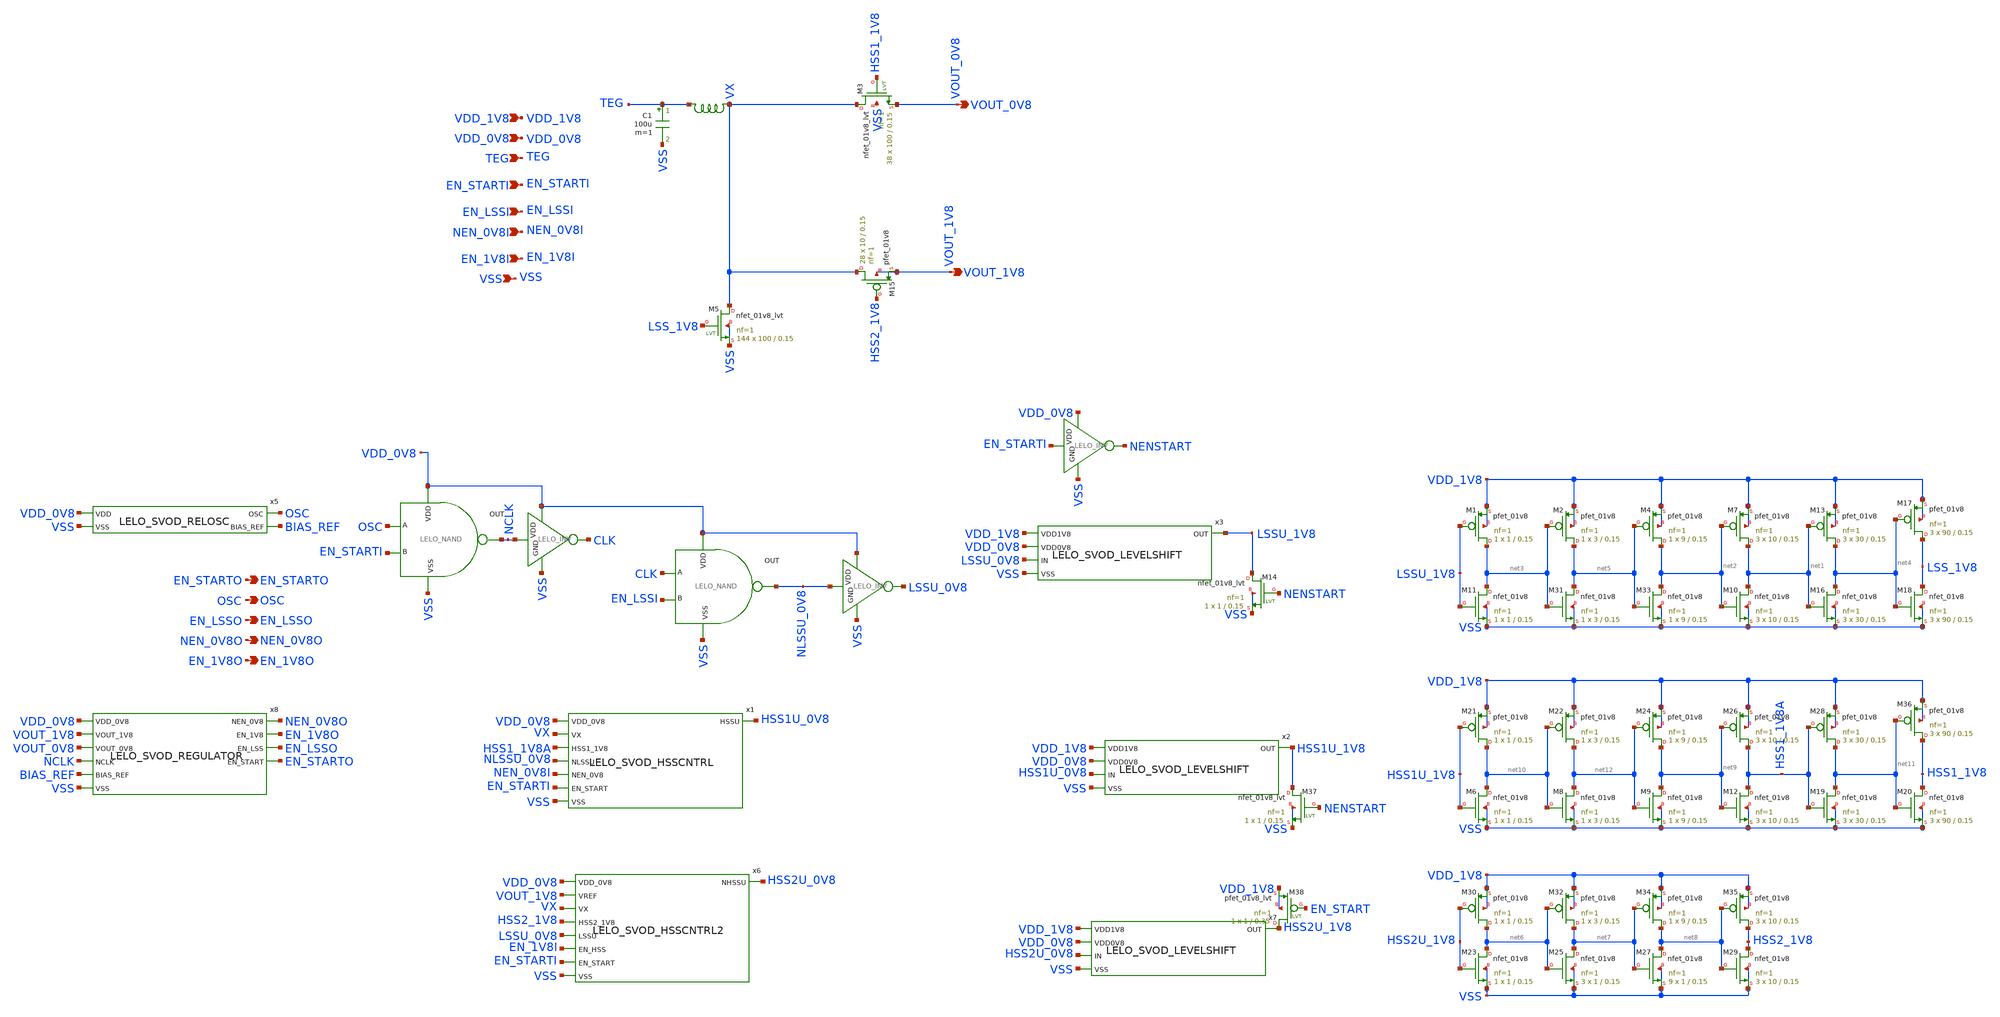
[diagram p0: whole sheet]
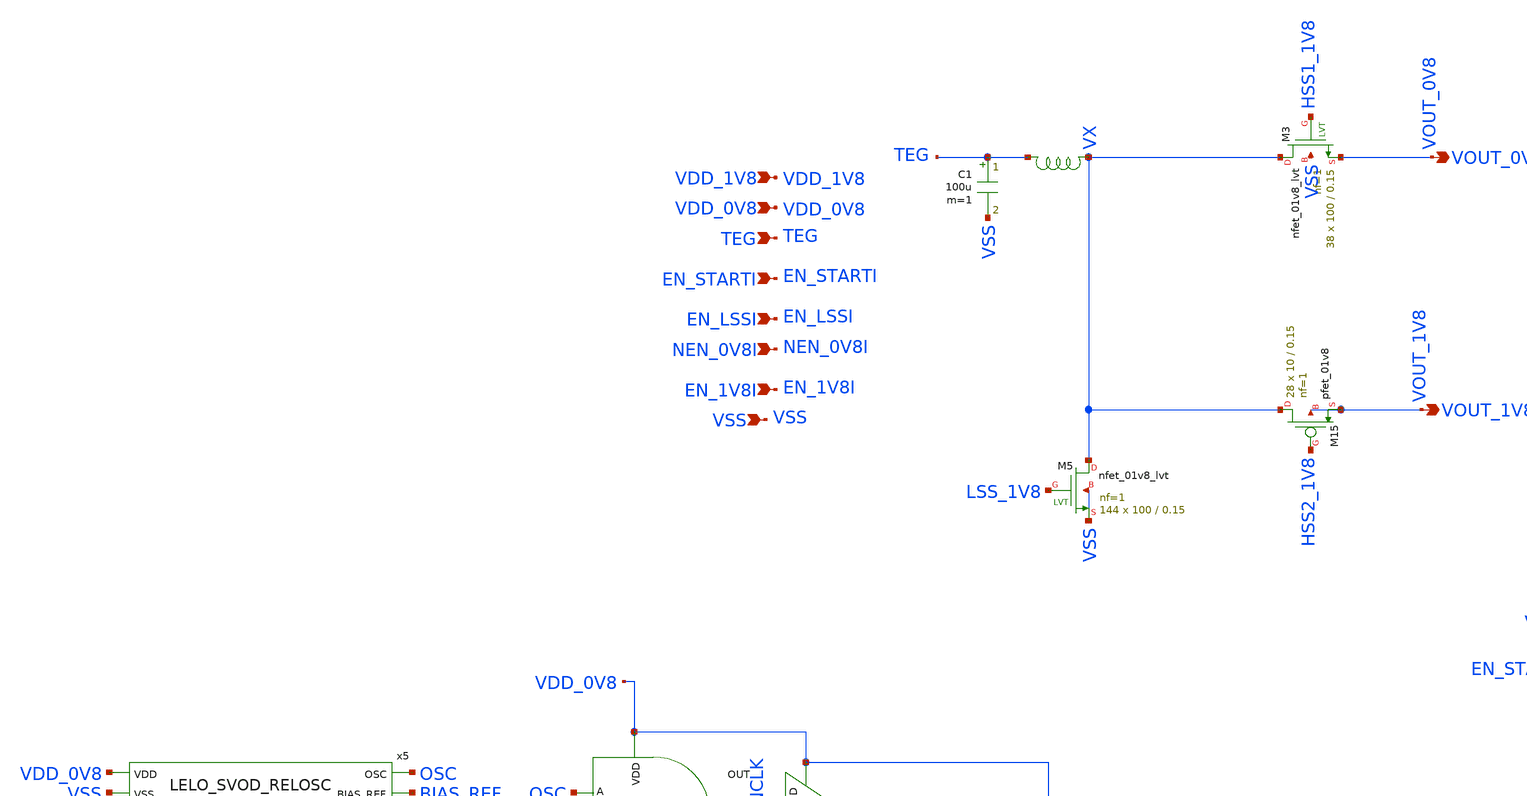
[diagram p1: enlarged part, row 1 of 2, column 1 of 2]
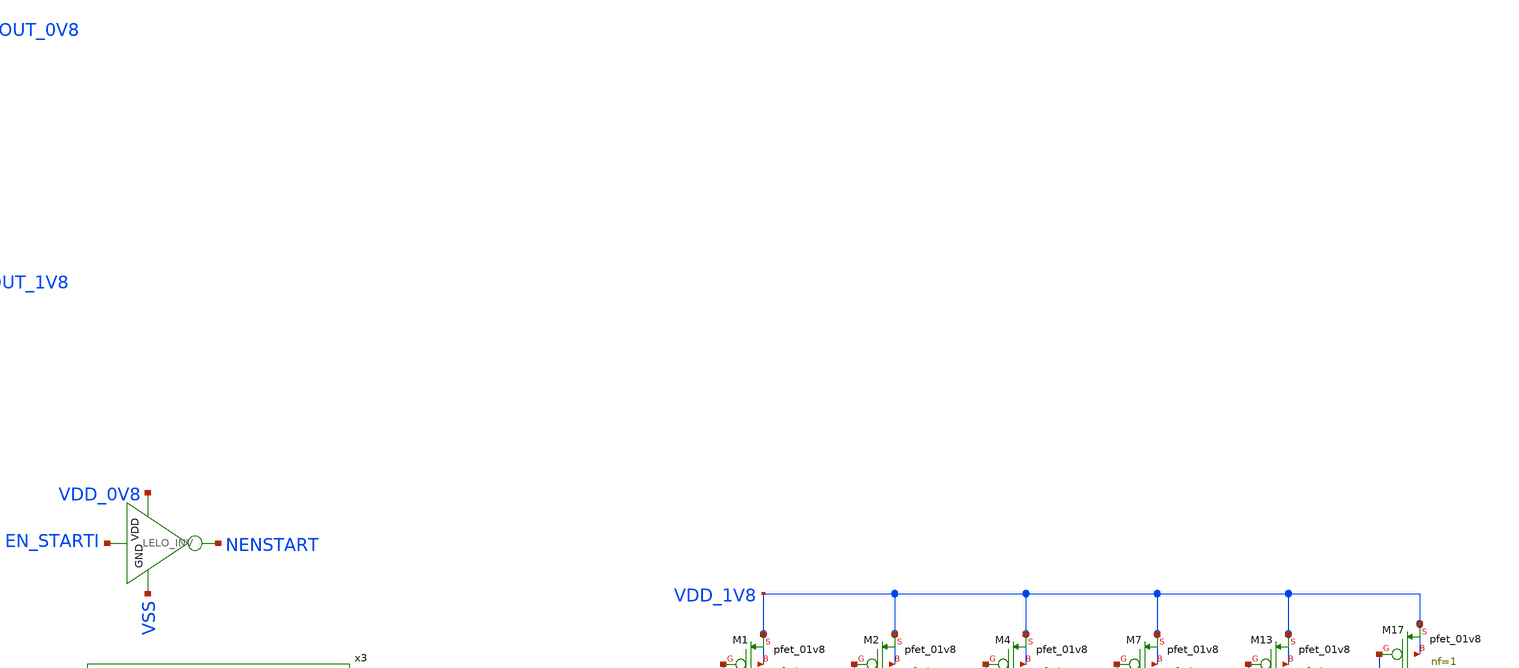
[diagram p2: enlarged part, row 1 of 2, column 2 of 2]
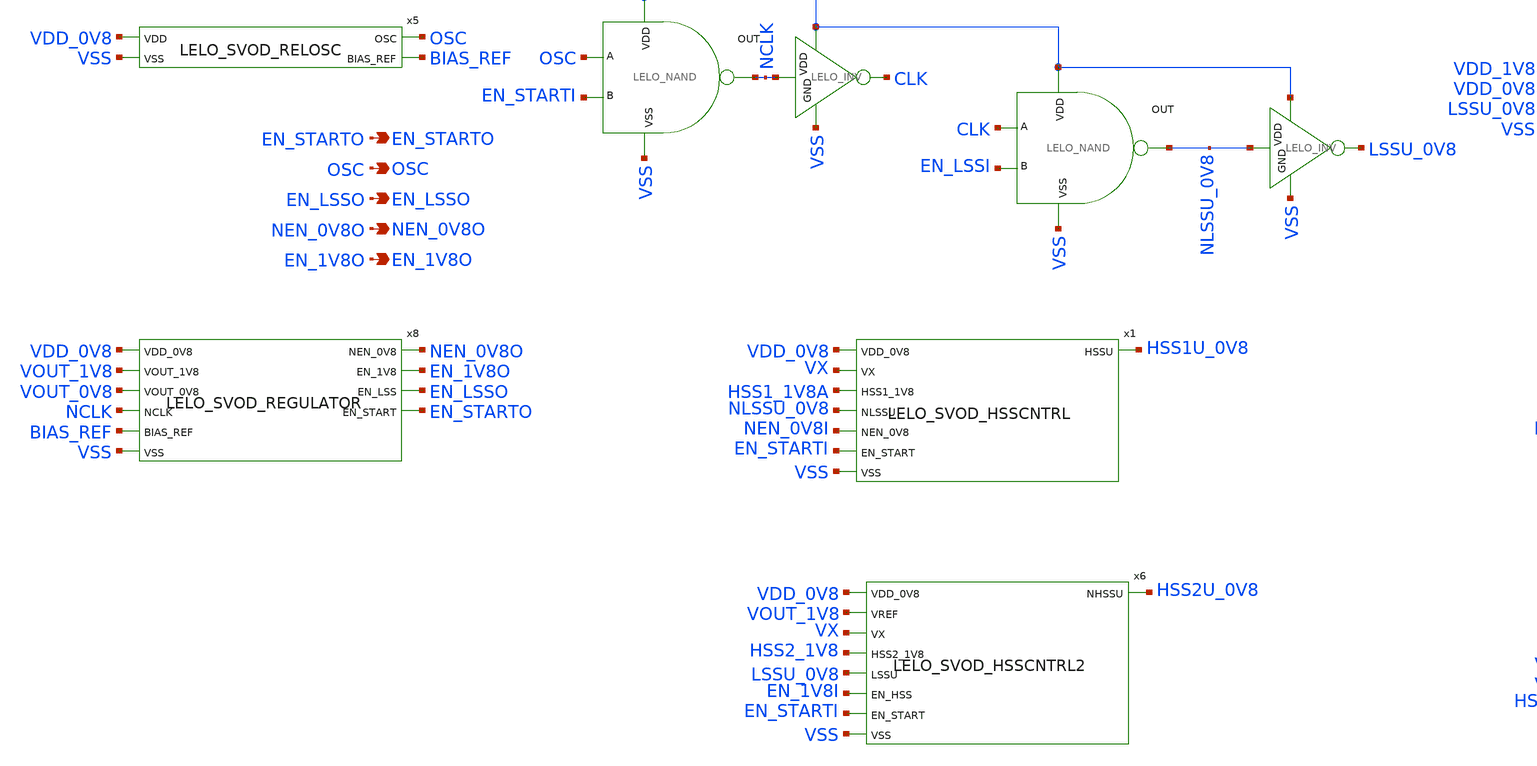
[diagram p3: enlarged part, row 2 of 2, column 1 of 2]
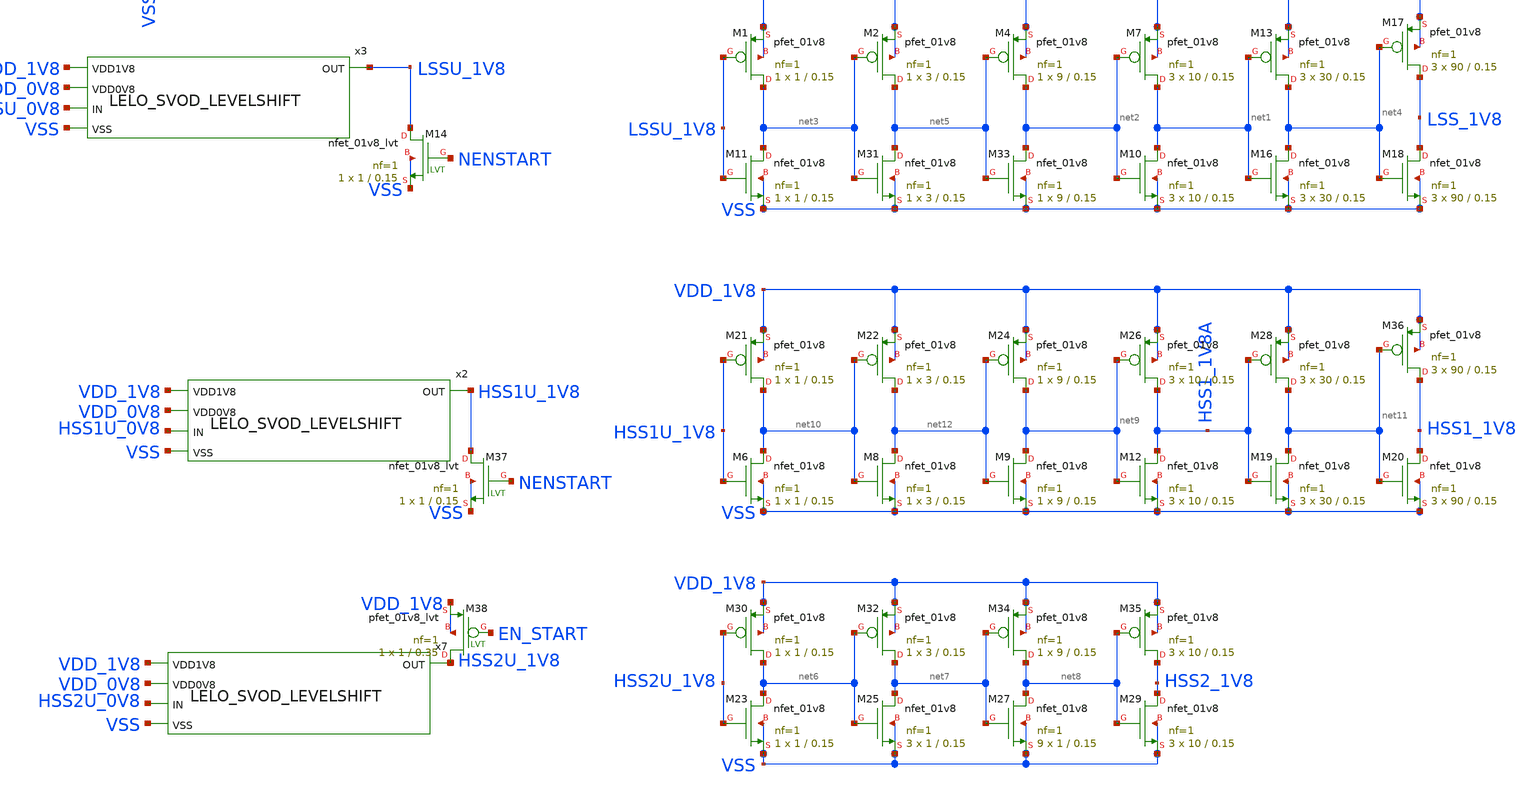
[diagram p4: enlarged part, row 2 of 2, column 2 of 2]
** sch_path: design/LELO_SVOD_SKY130A/LELO_SVOD_BOOST_2.sch
**.subckt LELO_SVOD_BOOST_2 VSS TEG VDD_0V8 VDD_1V8 VOUT_0V8 VOUT_1V8 EN_STARTO OSC EN_LSSO NEN_0V8O
*+ EN_1V8O EN_STARTI EN_LSSI NEN_0V8I EN_1V8I
*.ipin VSS
*.ipin TEG
*.ipin VDD_0V8
*.ipin VDD_1V8
*.opin VOUT_0V8
*.opin VOUT_1V8
*.opin EN_STARTO
*.opin OSC
*.opin EN_LSSO
*.opin NEN_0V8O
*.opin EN_1V8O
*.ipin EN_STARTI
*.ipin EN_LSSI
*.ipin NEN_0V8I
*.ipin EN_1V8I
C1 TEG VSS 100u m=1
XM5 VX LSS_1V8 VSS VSS sky130_fd_pr__nfet_01v8_lvt L=0.15 W=100 nf=1 ad='int((1 + 1)/2) * 100 / 1 * 0.29'
+ as='int((1 + 2)/2) * 100 / 1 * 0.29' pd='2*int((1 + 1)/2) * (100 / 1 + 0.29)' ps='2*int((1 + 2)/2) * (100 / 1 + 0.29)'
+ nrd='0.29 / 100 ' nrs='0.29 / 100 ' sa=0 sb=0 sd=0 mult=144 m=144
XM11 net3 LSSU_1V8 VSS VSS sky130_fd_pr__nfet_01v8 L=0.15 W=1 nf=1 ad='int((1 + 1)/2) * 1 / 1 * 0.29'
+ as='int((1 + 2)/2) * 1 / 1 * 0.29' pd='2*int((1 + 1)/2) * (1 / 1 + 0.29)' ps='2*int((1 + 2)/2) * (1 / 1 + 0.29)'
+ nrd='0.29 / 1 ' nrs='0.29 / 1 ' sa=0 sb=0 sd=0 mult=1 m=1
XM31 net5 net3 VSS VSS sky130_fd_pr__nfet_01v8 L=0.15 W=3 nf=1 ad='int((1 + 1)/2) * 3 / 1 * 0.29' as='int((1 + 2)/2) * 3 / 1 * 0.29'
+ pd='2*int((1 + 1)/2) * (3 / 1 + 0.29)' ps='2*int((1 + 2)/2) * (3 / 1 + 0.29)' nrd='0.29 / 3 ' nrs='0.29 / 3 '
+ sa=0 sb=0 sd=0 mult=1 m=1
XM33 net2 net5 VSS VSS sky130_fd_pr__nfet_01v8 L=0.15 W=9 nf=1 ad='int((1 + 1)/2) * 9 / 1 * 0.29' as='int((1 + 2)/2) * 9 / 1 * 0.29'
+ pd='2*int((1 + 1)/2) * (9 / 1 + 0.29)' ps='2*int((1 + 2)/2) * (9 / 1 + 0.29)' nrd='0.29 / 9 ' nrs='0.29 / 9 '
+ sa=0 sb=0 sd=0 mult=1 m=1
XM3 VX HSS1_1V8 VOUT_0V8 VSS sky130_fd_pr__nfet_01v8_lvt L=0.15 W=100 nf=1 ad='int((1 + 1)/2) * 100 / 1 * 0.29'
+ as='int((1 + 2)/2) * 100 / 1 * 0.29' pd='2*int((1 + 1)/2) * (100 / 1 + 0.29)' ps='2*int((1 + 2)/2) * (100 / 1 + 0.29)'
+ nrd='0.29 / 100 ' nrs='0.29 / 100 ' sa=0 sb=0 sd=0 mult=38 m=38
x1 HSS1U_0V8 VDD_0V8 VX HSS1_1V8A NLSSU_0V8 NEN_0V8I EN_STARTI VSS LELO_SVOD_HSSCNTRL
x2 VDD_1V8 HSS1U_1V8 VDD_0V8 HSS1U_0V8 VSS LELO_SVOD_LEVELSHIFT
x3 VDD_1V8 LSSU_1V8 VDD_0V8 LSSU_0V8 VSS LELO_SVOD_LEVELSHIFT
x4 VX TEG XGL6030-183_sat
x5 VDD_0V8 OSC BIAS_REF VSS LELO_SVOD_RELOSC
XM15 VX HSS2_1V8 VOUT_1V8 VOUT_1V8 sky130_fd_pr__pfet_01v8 L=0.15 W=10 nf=1 ad='int((1 + 1)/2) * 10 / 1 * 0.29'
+ as='int((1 + 2)/2) * 10 / 1 * 0.29' pd='2*int((1 + 1)/2) * (10 / 1 + 0.29)' ps='2*int((1 + 2)/2) * (10 / 1 + 0.29)'
+ nrd='0.29 / 10 ' nrs='0.29 / 10 ' sa=0 sb=0 sd=0 mult=28 m=28
x6 VDD_0V8 HSS2U_0V8 VOUT_1V8 VX HSS2_1V8 LSSU_0V8 EN_1V8I EN_STARTI VSS LELO_SVOD_HSSCNTRL2
x7 VDD_1V8 HSS2U_1V8 VDD_0V8 HSS2U_0V8 VSS LELO_SVOD_LEVELSHIFT
XM23 net6 HSS2U_1V8 VSS VSS sky130_fd_pr__nfet_01v8 L=0.15 W=1 nf=1 ad='int((1 + 1)/2) * 1 / 1 * 0.29'
+ as='int((1 + 2)/2) * 1 / 1 * 0.29' pd='2*int((1 + 1)/2) * (1 / 1 + 0.29)' ps='2*int((1 + 2)/2) * (1 / 1 + 0.29)'
+ nrd='0.29 / 1 ' nrs='0.29 / 1 ' sa=0 sb=0 sd=0 mult=1 m=1
XM25 net7 net6 VSS VSS sky130_fd_pr__nfet_01v8 L=0.15 W=1 nf=1 ad='int((1 + 1)/2) * 1 / 1 * 0.29' as='int((1 + 2)/2) * 1 / 1 * 0.29'
+ pd='2*int((1 + 1)/2) * (1 / 1 + 0.29)' ps='2*int((1 + 2)/2) * (1 / 1 + 0.29)' nrd='0.29 / 1 ' nrs='0.29 / 1 '
+ sa=0 sb=0 sd=0 mult=3 m=3
XM27 net8 net7 VSS VSS sky130_fd_pr__nfet_01v8 L=0.15 W=1 nf=1 ad='int((1 + 1)/2) * 1 / 1 * 0.29' as='int((1 + 2)/2) * 1 / 1 * 0.29'
+ pd='2*int((1 + 1)/2) * (1 / 1 + 0.29)' ps='2*int((1 + 2)/2) * (1 / 1 + 0.29)' nrd='0.29 / 1 ' nrs='0.29 / 1 '
+ sa=0 sb=0 sd=0 mult=9 m=9
XM29 HSS2_1V8 net8 VSS VSS sky130_fd_pr__nfet_01v8 L=0.15 W=10 nf=1 ad='int((1 + 1)/2) * 10 / 1 * 0.29'
+ as='int((1 + 2)/2) * 10 / 1 * 0.29' pd='2*int((1 + 1)/2) * (10 / 1 + 0.29)' ps='2*int((1 + 2)/2) * (10 / 1 + 0.29)'
+ nrd='0.29 / 10 ' nrs='0.29 / 10 ' sa=0 sb=0 sd=0 mult=3 m=3
x8 NEN_0V8O EN_1V8O EN_LSSO VDD_0V8 EN_STARTO VOUT_1V8 VOUT_0V8 NCLK BIAS_REF VSS
+ LELO_SVOD_REGULATOR
x9 VDD_0V8 NLSSU_0V8 CLK EN_LSSI VSS LELO_NAND
x10 VDD_0V8 NLSSU_0V8 LSSU_0V8 VSS LELO_INV
x11 VDD_0V8 NCLK CLK VSS LELO_INV
x13 VDD_0V8 NCLK OSC EN_STARTI VSS LELO_NAND
XM14 LSSU_1V8 NENSTART VSS VSS sky130_fd_pr__nfet_01v8_lvt L=0.15 W=1 nf=1 ad='int((1 + 1)/2) * 1 / 1 * 0.29'
+ as='int((1 + 2)/2) * 1 / 1 * 0.29' pd='2*int((1 + 1)/2) * (1 / 1 + 0.29)' ps='2*int((1 + 2)/2) * (1 / 1 + 0.29)'
+ nrd='0.29 / 1 ' nrs='0.29 / 1 ' sa=0 sb=0 sd=0 mult=1 m=1
XM10 net1 net2 VSS VSS sky130_fd_pr__nfet_01v8 L=0.15 W=10 nf=1 ad='int((1 + 1)/2) * 10 / 1 * 0.29' as='int((1 + 2)/2) * 10 / 1 * 0.29'
+ pd='2*int((1 + 1)/2) * (10 / 1 + 0.29)' ps='2*int((1 + 2)/2) * (10 / 1 + 0.29)' nrd='0.29 / 10 ' nrs='0.29 / 10 '
+ sa=0 sb=0 sd=0 mult=3 m=3
XM16 net4 net1 VSS VSS sky130_fd_pr__nfet_01v8 L=0.15 W=30 nf=1 ad='int((1 + 1)/2) * 30 / 1 * 0.29' as='int((1 + 2)/2) * 30 / 1 * 0.29'
+ pd='2*int((1 + 1)/2) * (30 / 1 + 0.29)' ps='2*int((1 + 2)/2) * (30 / 1 + 0.29)' nrd='0.29 / 30 ' nrs='0.29 / 30 '
+ sa=0 sb=0 sd=0 mult=3 m=3
XM18 LSS_1V8 net4 VSS VSS sky130_fd_pr__nfet_01v8 L=0.15 W=90 nf=1 ad='int((1 + 1)/2) * 90 / 1 * 0.29'
+ as='int((1 + 2)/2) * 90 / 1 * 0.29' pd='2*int((1 + 1)/2) * (90 / 1 + 0.29)' ps='2*int((1 + 2)/2) * (90 / 1 + 0.29)'
+ nrd='0.29 / 90 ' nrs='0.29 / 90 ' sa=0 sb=0 sd=0 mult=3 m=3
XM37 HSS1U_1V8 NENSTART VSS VSS sky130_fd_pr__nfet_01v8_lvt L=0.15 W=1 nf=1 ad='int((1 + 1)/2) * 1 / 1 * 0.29'
+ as='int((1 + 2)/2) * 1 / 1 * 0.29' pd='2*int((1 + 1)/2) * (1 / 1 + 0.29)' ps='2*int((1 + 2)/2) * (1 / 1 + 0.29)'
+ nrd='0.29 / 1 ' nrs='0.29 / 1 ' sa=0 sb=0 sd=0 mult=1 m=1
XM38 HSS2U_1V8 EN_START VDD_1V8 VDD_1V8 sky130_fd_pr__pfet_01v8_lvt L=0.35 W=1 nf=1 ad='int((1 + 1)/2) * 1 / 1 * 0.29'
+ as='int((1 + 2)/2) * 1 / 1 * 0.29' pd='2*int((1 + 1)/2) * (1 / 1 + 0.29)' ps='2*int((1 + 2)/2) * (1 / 1 + 0.29)'
+ nrd='0.29 / 1 ' nrs='0.29 / 1 ' sa=0 sb=0 sd=0 mult=1 m=1
x12 VDD_0V8 EN_STARTI NENSTART VSS LELO_INV
XM1 net3 LSSU_1V8 VDD_1V8 VDD_1V8 sky130_fd_pr__pfet_01v8 L=0.15 W=1 nf=1 ad='int((1 + 1)/2) * 1 / 1 * 0.29'
+ as='int((1 + 2)/2) * 1 / 1 * 0.29' pd='2*int((1 + 1)/2) * (1 / 1 + 0.29)' ps='2*int((1 + 2)/2) * (1 / 1 + 0.29)'
+ nrd='0.29 / 1 ' nrs='0.29 / 1 ' sa=0 sb=0 sd=0 mult=1 m=1
XM2 net5 net3 VDD_1V8 VDD_1V8 sky130_fd_pr__pfet_01v8 L=0.15 W=3 nf=1 ad='int((1 + 1)/2) * 3 / 1 * 0.29'
+ as='int((1 + 2)/2) * 3 / 1 * 0.29' pd='2*int((1 + 1)/2) * (3 / 1 + 0.29)' ps='2*int((1 + 2)/2) * (3 / 1 + 0.29)'
+ nrd='0.29 / 3 ' nrs='0.29 / 3 ' sa=0 sb=0 sd=0 mult=1 m=1
XM4 net2 net5 VDD_1V8 VDD_1V8 sky130_fd_pr__pfet_01v8 L=0.15 W=9 nf=1 ad='int((1 + 1)/2) * 9 / 1 * 0.29'
+ as='int((1 + 2)/2) * 9 / 1 * 0.29' pd='2*int((1 + 1)/2) * (9 / 1 + 0.29)' ps='2*int((1 + 2)/2) * (9 / 1 + 0.29)'
+ nrd='0.29 / 9 ' nrs='0.29 / 9 ' sa=0 sb=0 sd=0 mult=1 m=1
XM7 net1 net2 VDD_1V8 VDD_1V8 sky130_fd_pr__pfet_01v8 L=0.15 W=10 nf=1 ad='int((1 + 1)/2) * 10 / 1 * 0.29'
+ as='int((1 + 2)/2) * 10 / 1 * 0.29' pd='2*int((1 + 1)/2) * (10 / 1 + 0.29)' ps='2*int((1 + 2)/2) * (10 / 1 + 0.29)'
+ nrd='0.29 / 10 ' nrs='0.29 / 10 ' sa=0 sb=0 sd=0 mult=3 m=3
XM13 net4 net1 VDD_1V8 VDD_1V8 sky130_fd_pr__pfet_01v8 L=0.15 W=30 nf=1 ad='int((1 + 1)/2) * 30 / 1 * 0.29'
+ as='int((1 + 2)/2) * 30 / 1 * 0.29' pd='2*int((1 + 1)/2) * (30 / 1 + 0.29)' ps='2*int((1 + 2)/2) * (30 / 1 + 0.29)'
+ nrd='0.29 / 30 ' nrs='0.29 / 30 ' sa=0 sb=0 sd=0 mult=3 m=3
XM17 LSS_1V8 net4 VDD_1V8 VDD_1V8 sky130_fd_pr__pfet_01v8 L=0.15 W=90 nf=1 ad='int((1 + 1)/2) * 90 / 1 * 0.29'
+ as='int((1 + 2)/2) * 90 / 1 * 0.29' pd='2*int((1 + 1)/2) * (90 / 1 + 0.29)' ps='2*int((1 + 2)/2) * (90 / 1 + 0.29)'
+ nrd='0.29 / 90 ' nrs='0.29 / 90 ' sa=0 sb=0 sd=0 mult=3 m=3
XM6 net10 HSS1U_1V8 VSS VSS sky130_fd_pr__nfet_01v8 L=0.15 W=1 nf=1 ad='int((1 + 1)/2) * 1 / 1 * 0.29'
+ as='int((1 + 2)/2) * 1 / 1 * 0.29' pd='2*int((1 + 1)/2) * (1 / 1 + 0.29)' ps='2*int((1 + 2)/2) * (1 / 1 + 0.29)'
+ nrd='0.29 / 1 ' nrs='0.29 / 1 ' sa=0 sb=0 sd=0 mult=1 m=1
XM8 net12 net10 VSS VSS sky130_fd_pr__nfet_01v8 L=0.15 W=3 nf=1 ad='int((1 + 1)/2) * 3 / 1 * 0.29' as='int((1 + 2)/2) * 3 / 1 * 0.29'
+ pd='2*int((1 + 1)/2) * (3 / 1 + 0.29)' ps='2*int((1 + 2)/2) * (3 / 1 + 0.29)' nrd='0.29 / 3 ' nrs='0.29 / 3 '
+ sa=0 sb=0 sd=0 mult=1 m=1
XM9 net9 net12 VSS VSS sky130_fd_pr__nfet_01v8 L=0.15 W=9 nf=1 ad='int((1 + 1)/2) * 9 / 1 * 0.29' as='int((1 + 2)/2) * 9 / 1 * 0.29'
+ pd='2*int((1 + 1)/2) * (9 / 1 + 0.29)' ps='2*int((1 + 2)/2) * (9 / 1 + 0.29)' nrd='0.29 / 9 ' nrs='0.29 / 9 '
+ sa=0 sb=0 sd=0 mult=1 m=1
XM12 HSS1_1V8A net9 VSS VSS sky130_fd_pr__nfet_01v8 L=0.15 W=10 nf=1 ad='int((1 + 1)/2) * 10 / 1 * 0.29'
+ as='int((1 + 2)/2) * 10 / 1 * 0.29' pd='2*int((1 + 1)/2) * (10 / 1 + 0.29)' ps='2*int((1 + 2)/2) * (10 / 1 + 0.29)'
+ nrd='0.29 / 10 ' nrs='0.29 / 10 ' sa=0 sb=0 sd=0 mult=3 m=3
XM19 net11 HSS1_1V8A VSS VSS sky130_fd_pr__nfet_01v8 L=0.15 W=30 nf=1 ad='int((1 + 1)/2) * 30 / 1 * 0.29'
+ as='int((1 + 2)/2) * 30 / 1 * 0.29' pd='2*int((1 + 1)/2) * (30 / 1 + 0.29)' ps='2*int((1 + 2)/2) * (30 / 1 + 0.29)'
+ nrd='0.29 / 30 ' nrs='0.29 / 30 ' sa=0 sb=0 sd=0 mult=3 m=3
XM20 HSS1_1V8 net11 VSS VSS sky130_fd_pr__nfet_01v8 L=0.15 W=90 nf=1 ad='int((1 + 1)/2) * 90 / 1 * 0.29'
+ as='int((1 + 2)/2) * 90 / 1 * 0.29' pd='2*int((1 + 1)/2) * (90 / 1 + 0.29)' ps='2*int((1 + 2)/2) * (90 / 1 + 0.29)'
+ nrd='0.29 / 90 ' nrs='0.29 / 90 ' sa=0 sb=0 sd=0 mult=3 m=3
XM21 net10 HSS1U_1V8 VDD_1V8 VDD_1V8 sky130_fd_pr__pfet_01v8 L=0.15 W=1 nf=1 ad='int((1 + 1)/2) * 1 / 1 * 0.29'
+ as='int((1 + 2)/2) * 1 / 1 * 0.29' pd='2*int((1 + 1)/2) * (1 / 1 + 0.29)' ps='2*int((1 + 2)/2) * (1 / 1 + 0.29)'
+ nrd='0.29 / 1 ' nrs='0.29 / 1 ' sa=0 sb=0 sd=0 mult=1 m=1
XM22 net12 net10 VDD_1V8 VDD_1V8 sky130_fd_pr__pfet_01v8 L=0.15 W=3 nf=1 ad='int((1 + 1)/2) * 3 / 1 * 0.29'
+ as='int((1 + 2)/2) * 3 / 1 * 0.29' pd='2*int((1 + 1)/2) * (3 / 1 + 0.29)' ps='2*int((1 + 2)/2) * (3 / 1 + 0.29)'
+ nrd='0.29 / 3 ' nrs='0.29 / 3 ' sa=0 sb=0 sd=0 mult=1 m=1
XM24 net9 net12 VDD_1V8 VDD_1V8 sky130_fd_pr__pfet_01v8 L=0.15 W=9 nf=1 ad='int((1 + 1)/2) * 9 / 1 * 0.29'
+ as='int((1 + 2)/2) * 9 / 1 * 0.29' pd='2*int((1 + 1)/2) * (9 / 1 + 0.29)' ps='2*int((1 + 2)/2) * (9 / 1 + 0.29)'
+ nrd='0.29 / 9 ' nrs='0.29 / 9 ' sa=0 sb=0 sd=0 mult=1 m=1
XM26 HSS1_1V8A net9 VDD_1V8 VDD_1V8 sky130_fd_pr__pfet_01v8 L=0.15 W=10 nf=1 ad='int((1 + 1)/2) * 10 / 1 * 0.29'
+ as='int((1 + 2)/2) * 10 / 1 * 0.29' pd='2*int((1 + 1)/2) * (10 / 1 + 0.29)' ps='2*int((1 + 2)/2) * (10 / 1 + 0.29)'
+ nrd='0.29 / 10 ' nrs='0.29 / 10 ' sa=0 sb=0 sd=0 mult=3 m=3
XM28 net11 HSS1_1V8A VDD_1V8 VDD_1V8 sky130_fd_pr__pfet_01v8 L=0.15 W=30 nf=1 ad='int((1 + 1)/2) * 30 / 1 * 0.29'
+ as='int((1 + 2)/2) * 30 / 1 * 0.29' pd='2*int((1 + 1)/2) * (30 / 1 + 0.29)' ps='2*int((1 + 2)/2) * (30 / 1 + 0.29)'
+ nrd='0.29 / 30 ' nrs='0.29 / 30 ' sa=0 sb=0 sd=0 mult=3 m=3
XM36 HSS1_1V8 net11 VDD_1V8 VDD_1V8 sky130_fd_pr__pfet_01v8 L=0.15 W=90 nf=1 ad='int((1 + 1)/2) * 90 / 1 * 0.29'
+ as='int((1 + 2)/2) * 90 / 1 * 0.29' pd='2*int((1 + 1)/2) * (90 / 1 + 0.29)' ps='2*int((1 + 2)/2) * (90 / 1 + 0.29)'
+ nrd='0.29 / 90 ' nrs='0.29 / 90 ' sa=0 sb=0 sd=0 mult=3 m=3
XM30 net6 HSS2U_1V8 VDD_1V8 VDD_1V8 sky130_fd_pr__pfet_01v8 L=0.15 W=1 nf=1 ad='int((1 + 1)/2) * 1 / 1 * 0.29'
+ as='int((1 + 2)/2) * 1 / 1 * 0.29' pd='2*int((1 + 1)/2) * (1 / 1 + 0.29)' ps='2*int((1 + 2)/2) * (1 / 1 + 0.29)'
+ nrd='0.29 / 1 ' nrs='0.29 / 1 ' sa=0 sb=0 sd=0 mult=1 m=1
XM32 net7 net6 VDD_1V8 VDD_1V8 sky130_fd_pr__pfet_01v8 L=0.15 W=3 nf=1 ad='int((1 + 1)/2) * 3 / 1 * 0.29'
+ as='int((1 + 2)/2) * 3 / 1 * 0.29' pd='2*int((1 + 1)/2) * (3 / 1 + 0.29)' ps='2*int((1 + 2)/2) * (3 / 1 + 0.29)'
+ nrd='0.29 / 3 ' nrs='0.29 / 3 ' sa=0 sb=0 sd=0 mult=1 m=1
XM34 net8 net7 VDD_1V8 VDD_1V8 sky130_fd_pr__pfet_01v8 L=0.15 W=9 nf=1 ad='int((1 + 1)/2) * 9 / 1 * 0.29'
+ as='int((1 + 2)/2) * 9 / 1 * 0.29' pd='2*int((1 + 1)/2) * (9 / 1 + 0.29)' ps='2*int((1 + 2)/2) * (9 / 1 + 0.29)'
+ nrd='0.29 / 9 ' nrs='0.29 / 9 ' sa=0 sb=0 sd=0 mult=1 m=1
XM35 HSS2_1V8 net8 VDD_1V8 VDD_1V8 sky130_fd_pr__pfet_01v8 L=0.15 W=10 nf=1 ad='int((1 + 1)/2) * 10 / 1 * 0.29'
+ as='int((1 + 2)/2) * 10 / 1 * 0.29' pd='2*int((1 + 1)/2) * (10 / 1 + 0.29)' ps='2*int((1 + 2)/2) * (10 / 1 + 0.29)'
+ nrd='0.29 / 10 ' nrs='0.29 / 10 ' sa=0 sb=0 sd=0 mult=3 m=3
**.ends
.end
